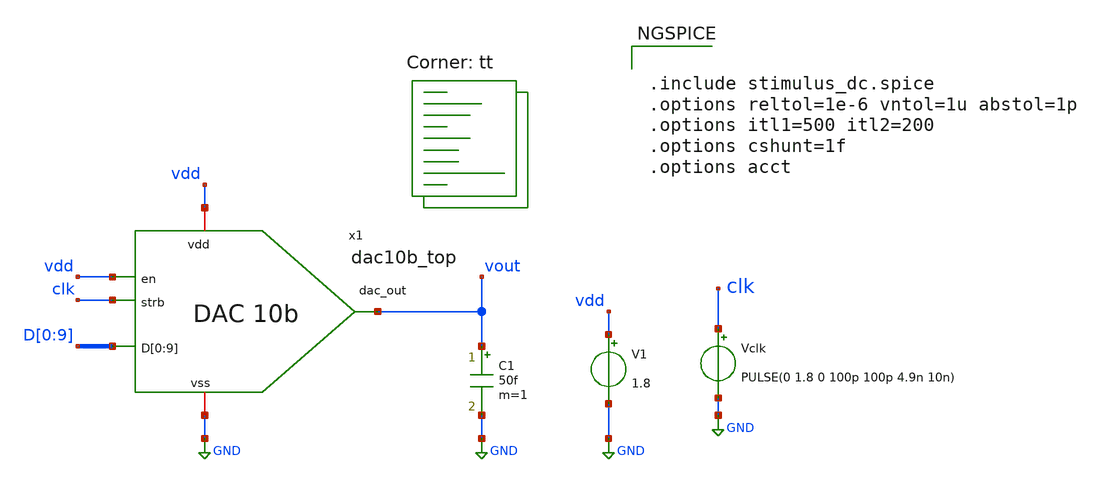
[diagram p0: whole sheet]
** sch_path: xschem/dac10b_top/ramp_tb/dac10b_top_tb_ramp.sch
**.subckt dac10b_top_tb_ramp
x1 vdd GND vdd clk D[0] D[1] D[2] D[3] D[4] D[5] D[6] D[7] D[8] D[9] vout dac10b_top
C1 vout GND 50f m=1
V1 vdd GND 1.8
Vclk clk GND PULSE(0 1.8 0 100p 100p 4.9n 10n)
**** begin user architecture code
.lib $::SKYWATER_MODELS/sky130.lib.spice tt


.include stimulus_dc.spice
.options reltol=1e-6 vntol=1u abstol=1p
.options itl1=500 itl2=200
.options cshunt=1f
.options acct


**** end user architecture code
**.ends
.GLOBAL GND
.end
